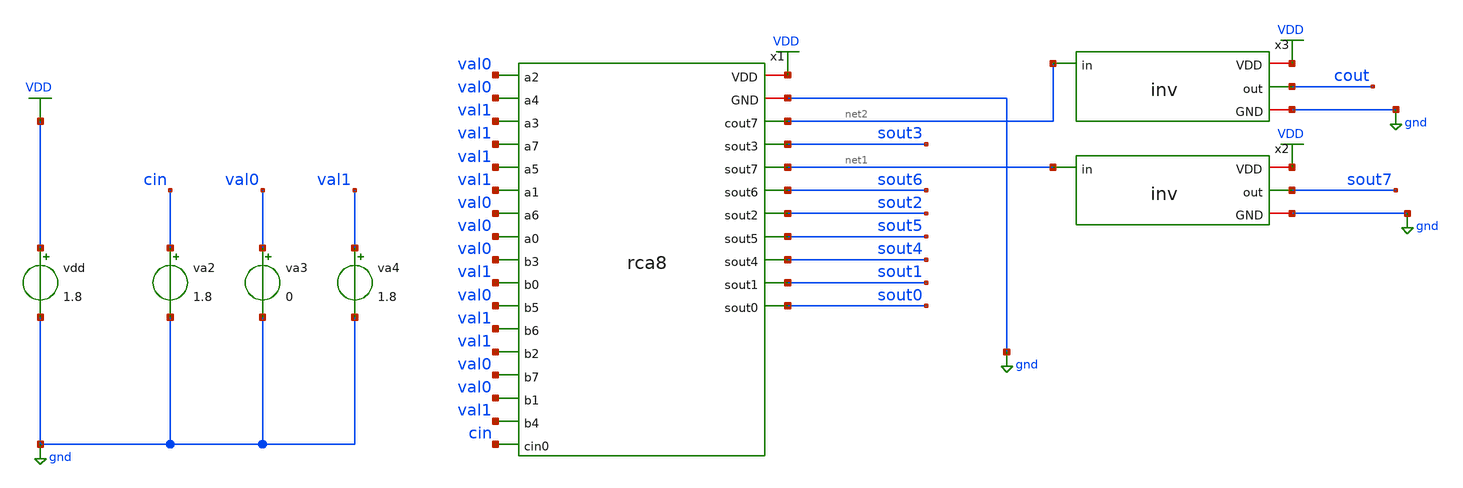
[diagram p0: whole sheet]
** sch_path: assignments/assignment8/assignrca1.sch
**.subckt assignrca1
x1 net2 cin val1 val0 val0 val1 val1 val0 val0 val1 val1 val0 val0 val1 val1 val0 val0 val1 sout0
+ sout1 sout2 sout3 sout4 sout5 sout6 net1 gnd VDD rca8
vdd VDD gnd 1.8
va3 val0 gnd 0
va4 val1 gnd 1.8
va2 cin gnd 1.8
x2 VDD net1 sout7 gnd inv
x3 VDD net2 cout gnd inv
**** begin user architecture code


.include rca8_extracted.spice
.control
* Set up the input pulse
alter @va2[pulse] = [ 0 1.8 0 10p 10p 4n 8n ]

* Extend transient time to 40n to avoid 'out of interval' errors
tran 1p 40n

* Measure critical path delay from cin to cout
meas tran delay_cin_cout TRIG v(cin) VAL=0.9 RISE=3 TARG v(cout) VAL=0.9 FALL=3

* Measure critical path delay from cin to MSB sum (sout7)
meas tran delay_cin_sout7 TRIG v(cin) VAL=0.9 RISE=3 TARG v(sout7) VAL=0.9 FALL=3

* Print the delay results for your summary table
print delay_cin_cout delay_cin_sout7
plot v(cin) v(cout)
.endc


.lib $::SKYWATER_MODELS/sky130.lib.spice tt
**** end user architecture code
**.ends

* expanding   symbol:  inv.sym # of pins=4
** sym_path: assignments/assignment6/inv.sym
** sch_path: assignments/assignment6/inv.sch
.subckt inv VDD in out GND
*.ipin in
*.iopin GND
*.iopin VDD
*.opin out
XM3 out in GND GND sky130_fd_pr__nfet_01v8 L=0.15 W=0.42 nf=1 ad='int((nf+1)/2) * W/nf * 0.29' as='int((nf+2)/2) * W/nf * 0.29'
+ pd='2*int((nf+1)/2) * (W/nf + 0.29)' ps='2*int((nf+2)/2) * (W/nf + 0.29)' nrd='0.29 / W' nrs='0.29 / W'
+ sa=0 sb=0 sd=0 mult=1 m=1
XM4 out in VDD VDD sky130_fd_pr__pfet_01v8 L=0.15 W=0.84 nf=1 ad='int((nf+1)/2) * W/nf * 0.29' as='int((nf+2)/2) * W/nf * 0.29'
+ pd='2*int((nf+1)/2) * (W/nf + 0.29)' ps='2*int((nf+2)/2) * (W/nf + 0.29)' nrd='0.29 / W' nrs='0.29 / W'
+ sa=0 sb=0 sd=0 mult=1 m=1
.ends

.GLOBAL VDD
.GLOBAL gnd
.end
